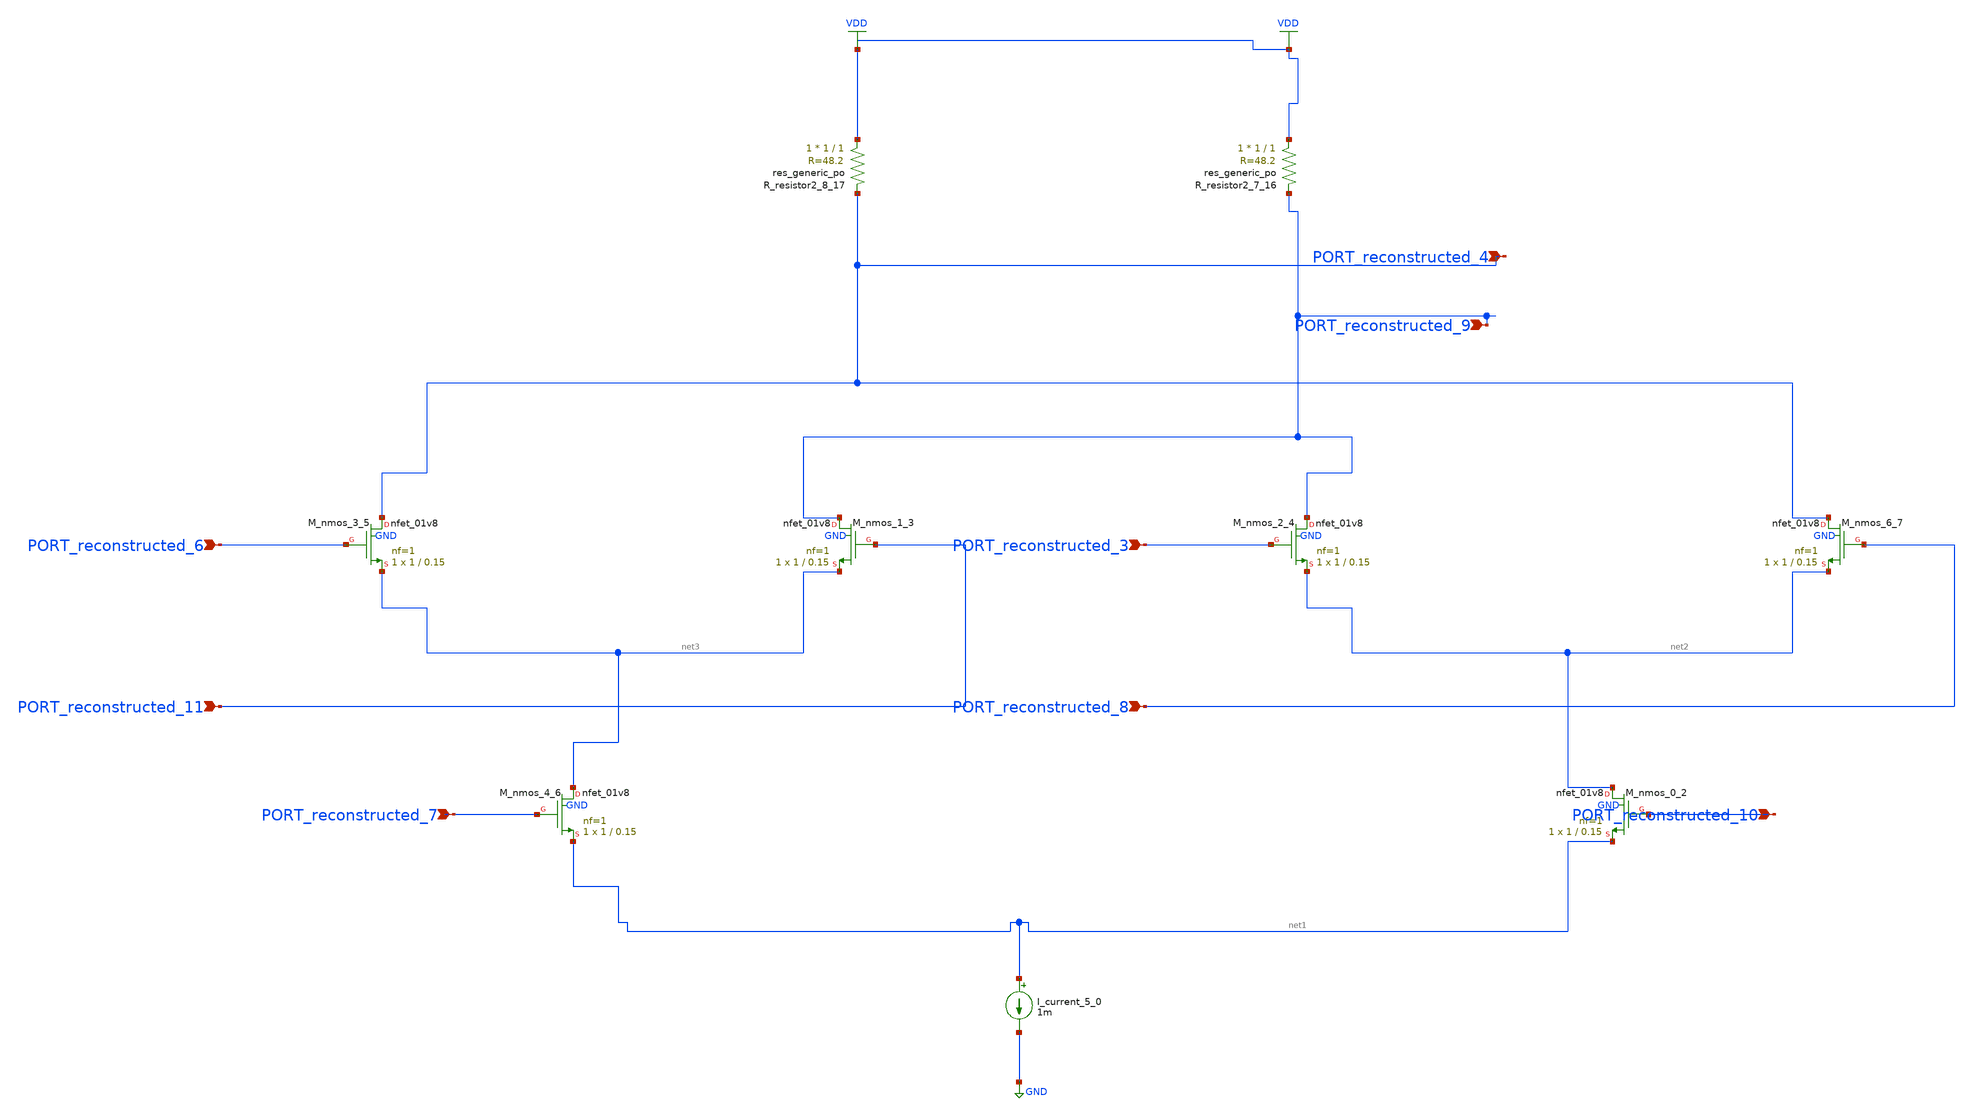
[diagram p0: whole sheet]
** sch_path: schematics/AMSNet/232.sch
**.subckt 232 PORT_reconstructed_7 PORT_reconstructed_9 PORT_reconstructed_6 PORT_reconstructed_10
*+ PORT_reconstructed_3 PORT_reconstructed_4 PORT_reconstructed_8 PORT_reconstructed_11
*.ipin PORT_reconstructed_7
*.ipin PORT_reconstructed_9
*.ipin PORT_reconstructed_6
*.ipin PORT_reconstructed_10
*.ipin PORT_reconstructed_3
*.ipin PORT_reconstructed_4
*.ipin PORT_reconstructed_8
*.ipin PORT_reconstructed_11
I_current_5_0 net1 GND 1m
XM_nmos_0_2 net2 PORT_reconstructed_10 net1 GND sky130_fd_pr__nfet_01v8 L=0.15 W=1 nf=1 ad='int((1 + 1)/2) * 1 / 1 * 0.29'
+ as='int((1 + 2)/2) * 1 / 1 * 0.29' pd='2*int((1 + 1)/2) * (1 / 1 + 0.29)' ps='2*int((1 + 2)/2) * (1 / 1 + 0.29)'
+ nrd='0.29 / 1 ' nrs='0.29 / 1 ' sa=0 sb=0 sd=0 mult=1 m=1
XM_nmos_1_3 PORT_reconstructed_9 PORT_reconstructed_11 net3 GND sky130_fd_pr__nfet_01v8 L=0.15 W=1 nf=1
+ ad='int((1 + 1)/2) * 1 / 1 * 0.29' as='int((1 + 2)/2) * 1 / 1 * 0.29' pd='2*int((1 + 1)/2) * (1 / 1 + 0.29)'
+ ps='2*int((1 + 2)/2) * (1 / 1 + 0.29)' nrd='0.29 / 1 ' nrs='0.29 / 1 ' sa=0 sb=0 sd=0 mult=1 m=1
XM_nmos_2_4 PORT_reconstructed_9 PORT_reconstructed_3 net2 GND sky130_fd_pr__nfet_01v8 L=0.15 W=1 nf=1
+ ad='int((1 + 1)/2) * 1 / 1 * 0.29' as='int((1 + 2)/2) * 1 / 1 * 0.29' pd='2*int((1 + 1)/2) * (1 / 1 + 0.29)'
+ ps='2*int((1 + 2)/2) * (1 / 1 + 0.29)' nrd='0.29 / 1 ' nrs='0.29 / 1 ' sa=0 sb=0 sd=0 mult=1 m=1
XM_nmos_3_5 PORT_reconstructed_4 PORT_reconstructed_6 net3 GND sky130_fd_pr__nfet_01v8 L=0.15 W=1 nf=1
+ ad='int((1 + 1)/2) * 1 / 1 * 0.29' as='int((1 + 2)/2) * 1 / 1 * 0.29' pd='2*int((1 + 1)/2) * (1 / 1 + 0.29)'
+ ps='2*int((1 + 2)/2) * (1 / 1 + 0.29)' nrd='0.29 / 1 ' nrs='0.29 / 1 ' sa=0 sb=0 sd=0 mult=1 m=1
XM_nmos_4_6 net3 PORT_reconstructed_7 net1 GND sky130_fd_pr__nfet_01v8 L=0.15 W=1 nf=1 ad='int((1 + 1)/2) * 1 / 1 * 0.29'
+ as='int((1 + 2)/2) * 1 / 1 * 0.29' pd='2*int((1 + 1)/2) * (1 / 1 + 0.29)' ps='2*int((1 + 2)/2) * (1 / 1 + 0.29)'
+ nrd='0.29 / 1 ' nrs='0.29 / 1 ' sa=0 sb=0 sd=0 mult=1 m=1
XM_nmos_6_7 PORT_reconstructed_4 PORT_reconstructed_8 net2 GND sky130_fd_pr__nfet_01v8 L=0.15 W=1 nf=1
+ ad='int((1 + 1)/2) * 1 / 1 * 0.29' as='int((1 + 2)/2) * 1 / 1 * 0.29' pd='2*int((1 + 1)/2) * (1 / 1 + 0.29)'
+ ps='2*int((1 + 2)/2) * (1 / 1 + 0.29)' nrd='0.29 / 1 ' nrs='0.29 / 1 ' sa=0 sb=0 sd=0 mult=1 m=1
XR_resistor2_7_16 VDD PORT_reconstructed_9 sky130_fd_pr__res_generic_po W=1 L=1 m=1
XR_resistor2_8_17 VDD PORT_reconstructed_4 sky130_fd_pr__res_generic_po W=1 L=1 m=1
**.ends
.GLOBAL GND
.GLOBAL VDD
.end
